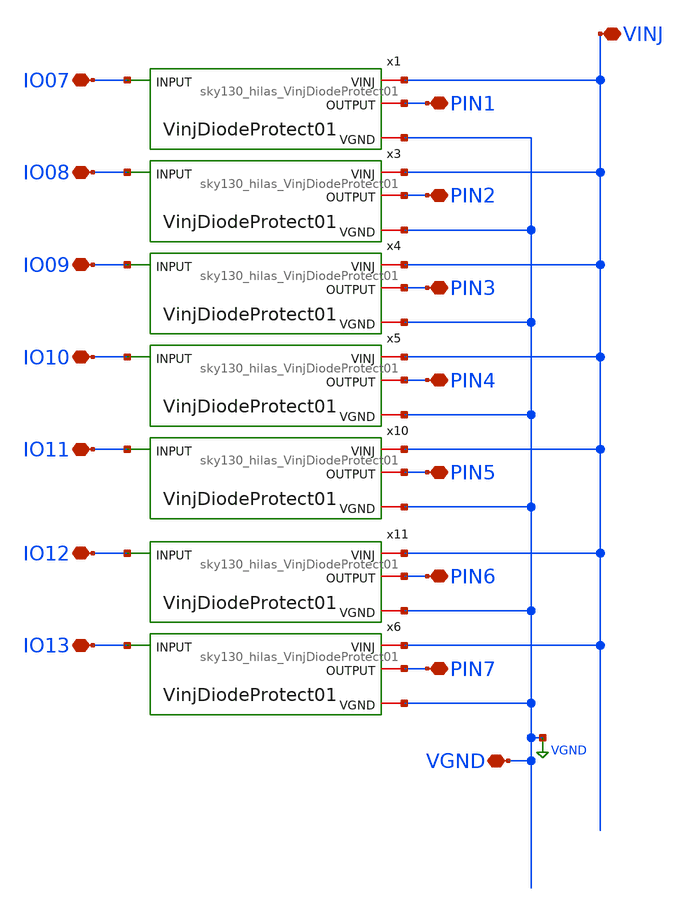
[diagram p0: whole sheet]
** sch_path: libs.ref/sky130_hilas_sc/xschem/sky130_hilas_RightProtection.sch
**.subckt sky130_hilas_RightProtection PIN1 IO07 IO08 IO09 IO10 IO11 IO12 IO13 PIN2 PIN3 PIN4 PIN5
*+ PIN6 PIN7 VINJ VGND
*.iopin PIN1
*.iopin IO07
*.iopin IO08
*.iopin IO09
*.iopin IO10
*.iopin IO11
*.iopin IO12
*.iopin IO13
*.iopin PIN2
*.iopin PIN3
*.iopin PIN4
*.iopin PIN5
*.iopin PIN6
*.iopin PIN7
*.iopin VINJ
*.iopin VGND
x1 VINJ PIN1 IO07 VGND sky130_hilas_VinjDiodeProtect01
x3 VINJ PIN2 IO08 VGND sky130_hilas_VinjDiodeProtect01
x4 VINJ PIN3 IO09 VGND sky130_hilas_VinjDiodeProtect01
x5 VINJ PIN4 IO10 VGND sky130_hilas_VinjDiodeProtect01
x6 VINJ PIN7 IO13 VGND sky130_hilas_VinjDiodeProtect01
x10 VINJ PIN5 IO11 VGND sky130_hilas_VinjDiodeProtect01
x11 VINJ PIN6 IO12 VGND sky130_hilas_VinjDiodeProtect01
**.ends

* expanding   symbol:  sky130_hilas_VinjDiodeProtect01.sym # of pins=4
** sym_path: libs.ref/sky130_hilas_sc/xschem/sky130_hilas_VinjDiodeProtect01.sym
** sch_path: libs.ref/sky130_hilas_sc/xschem/sky130_hilas_VinjDiodeProtect01.sch
.subckt sky130_hilas_VinjDiodeProtect01 VINJ OUTPUT INPUT VGND
*.ipin INPUT
*.iopin VINJ
*.iopin OUTPUT
*.iopin VGND
XD1 OUTPUT VINJ sky130_fd_pr__diode_pw2nd_05v5 area=1 pj=4e6
XD2 VGND OUTPUT sky130_fd_pr__diode_pw2nd_05v5 area=1 pj=4e6
R1 INPUT OUTPUT 100 m=1
.ends

.GLOBAL VGND
.end
